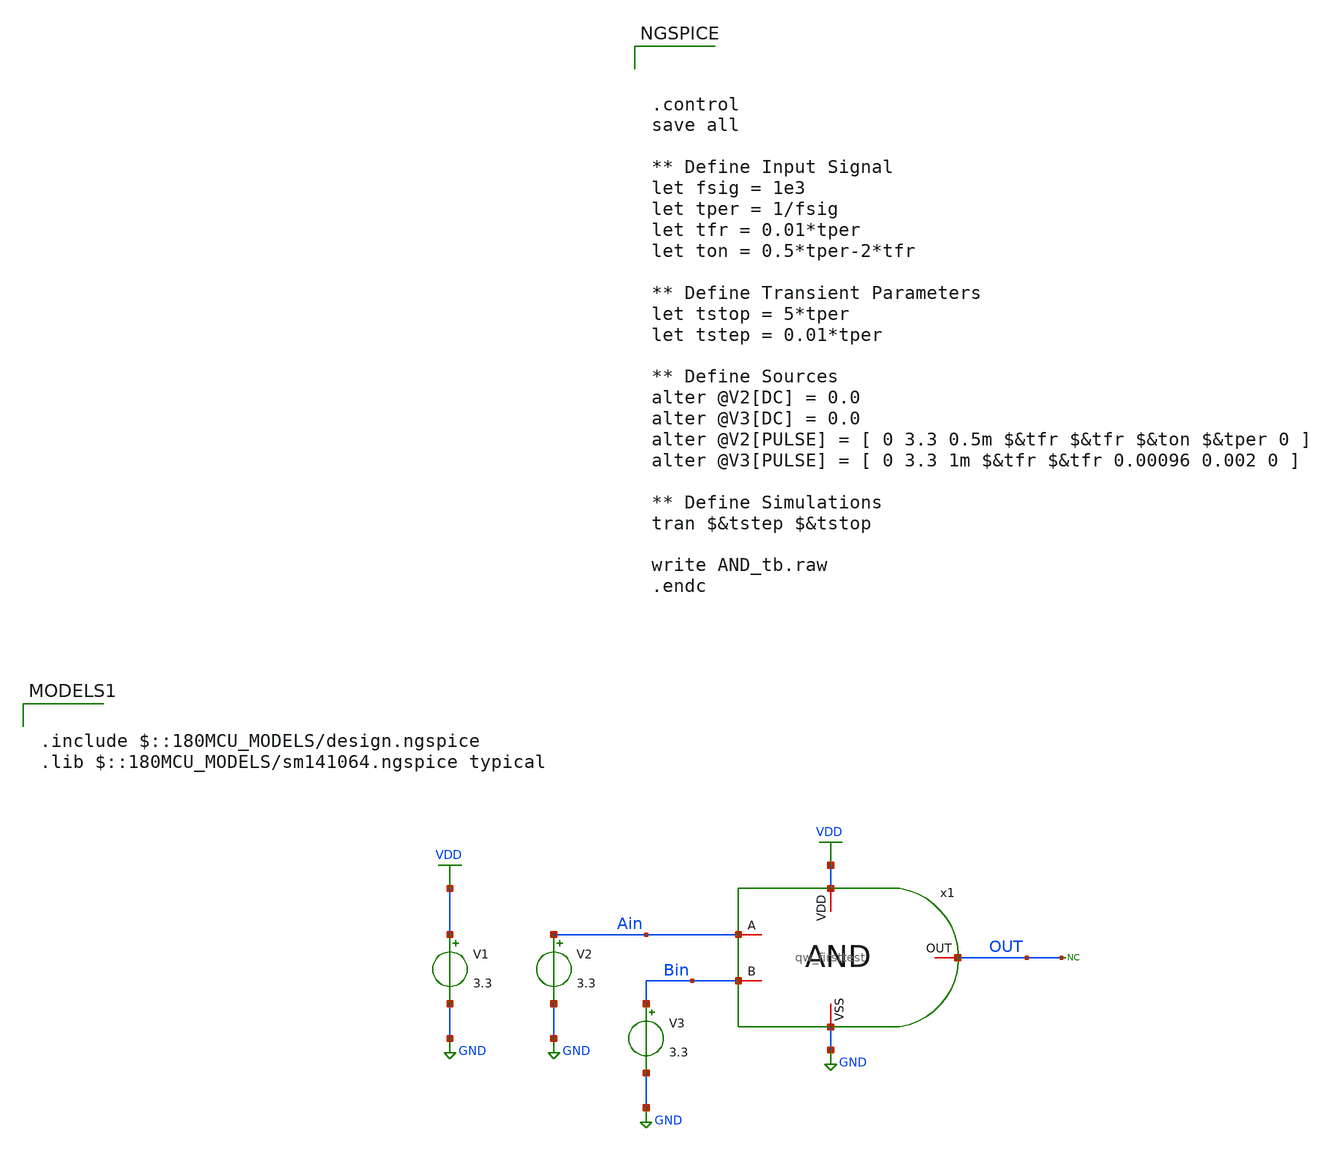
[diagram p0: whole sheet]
** sch_path: designs/libs/qw_core_analog_pkedit/AND_tb.sch
**.subckt AND_tb
x1 VDD OUT Ain Bin GND qw_firsttest
V1 VDD GND 3.3
* noconn OUT
V2 Ain GND 3.3
V3 Bin GND 3.3
**** begin user architecture code



.control
save all

** Define Input Signal
let fsig = 1e3
let tper = 1/fsig
let tfr = 0.01*tper
let ton = 0.5*tper-2*tfr

** Define Transient Parameters
let tstop = 5*tper
let tstep = 0.01*tper

** Define Sources
alter @V2[DC] = 0.0
alter @V3[DC] = 0.0
alter @V2[PULSE] = [ 0 3.3 0.5m $&tfr $&tfr $&ton $&tper 0 ]
alter @V3[PULSE] = [ 0 3.3 1m $&tfr $&tfr 0.00096 0.002 0 ]

** Define Simulations
tran $&tstep $&tstop

write AND_tb.raw
.endc



.include $::180MCU_MODELS/design.ngspice
.lib $::180MCU_MODELS/sm141064.ngspice typical

**** end user architecture code
**.ends

* expanding   symbol:  qw_firsttest.sym # of pins=5
** sym_path: designs/libs/core_analog/qw_AND/qw_firsttest.sym
** sch_path: designs/libs/core_analog/qw_AND/qw_firsttest.sch
.subckt qw_firsttest VDD OUT A B VSS
*.iopin VDD
*.iopin VSS
*.iopin B
*.iopin A
*.iopin OUT
XM1 AnandB A net1 VSS nfet_03v3 L=0.28u W=1u nf=1 ad='int((nf+1)/2) * W/nf * 0.18u' as='int((nf+2)/2) * W/nf * 0.18u'
+ pd='2*int((nf+1)/2) * (W/nf + 0.18u)' ps='2*int((nf+2)/2) * (W/nf + 0.18u)' nrd='0.18u / W' nrs='0.18u / W'
+ sa=0 sb=0 sd=0 m=1
XM2 AnandB A VDD VDD pfet_03v3 L=0.28u W=1u nf=1 ad='int((nf+1)/2) * W/nf * 0.18u' as='int((nf+2)/2) * W/nf * 0.18u'
+ pd='2*int((nf+1)/2) * (W/nf + 0.18u)' ps='2*int((nf+2)/2) * (W/nf + 0.18u)' nrd='0.18u / W' nrs='0.18u / W'
+ sa=0 sb=0 sd=0 m=1
XM3 net1 B VSS VSS nfet_03v3 L=0.28u W=1u nf=1 ad='int((nf+1)/2) * W/nf * 0.18u' as='int((nf+2)/2) * W/nf * 0.18u'
+ pd='2*int((nf+1)/2) * (W/nf + 0.18u)' ps='2*int((nf+2)/2) * (W/nf + 0.18u)' nrd='0.18u / W' nrs='0.18u / W'
+ sa=0 sb=0 sd=0 m=1
XM4 AnandB B VDD VDD pfet_03v3 L=0.28u W=1u nf=1 ad='int((nf+1)/2) * W/nf * 0.18u' as='int((nf+2)/2) * W/nf * 0.18u'
+ pd='2*int((nf+1)/2) * (W/nf + 0.18u)' ps='2*int((nf+2)/2) * (W/nf + 0.18u)' nrd='0.18u / W' nrs='0.18u / W'
+ sa=0 sb=0 sd=0 m=1
XM5 OUT AnandB VSS VSS nfet_03v3 L=0.28u W=0.5u nf=1 ad='int((nf+1)/2) * W/nf * 0.18u' as='int((nf+2)/2) * W/nf * 0.18u'
+ pd='2*int((nf+1)/2) * (W/nf + 0.18u)' ps='2*int((nf+2)/2) * (W/nf + 0.18u)' nrd='0.18u / W' nrs='0.18u / W'
+ sa=0 sb=0 sd=0 m=1
XM6 OUT AnandB VDD VDD pfet_03v3 L=0.28u W=1u nf=1 ad='int((nf+1)/2) * W/nf * 0.18u' as='int((nf+2)/2) * W/nf * 0.18u'
+ pd='2*int((nf+1)/2) * (W/nf + 0.18u)' ps='2*int((nf+2)/2) * (W/nf + 0.18u)' nrd='0.18u / W' nrs='0.18u / W'
+ sa=0 sb=0 sd=0 m=1
.ends

.GLOBAL GND
.GLOBAL VDD
.end
